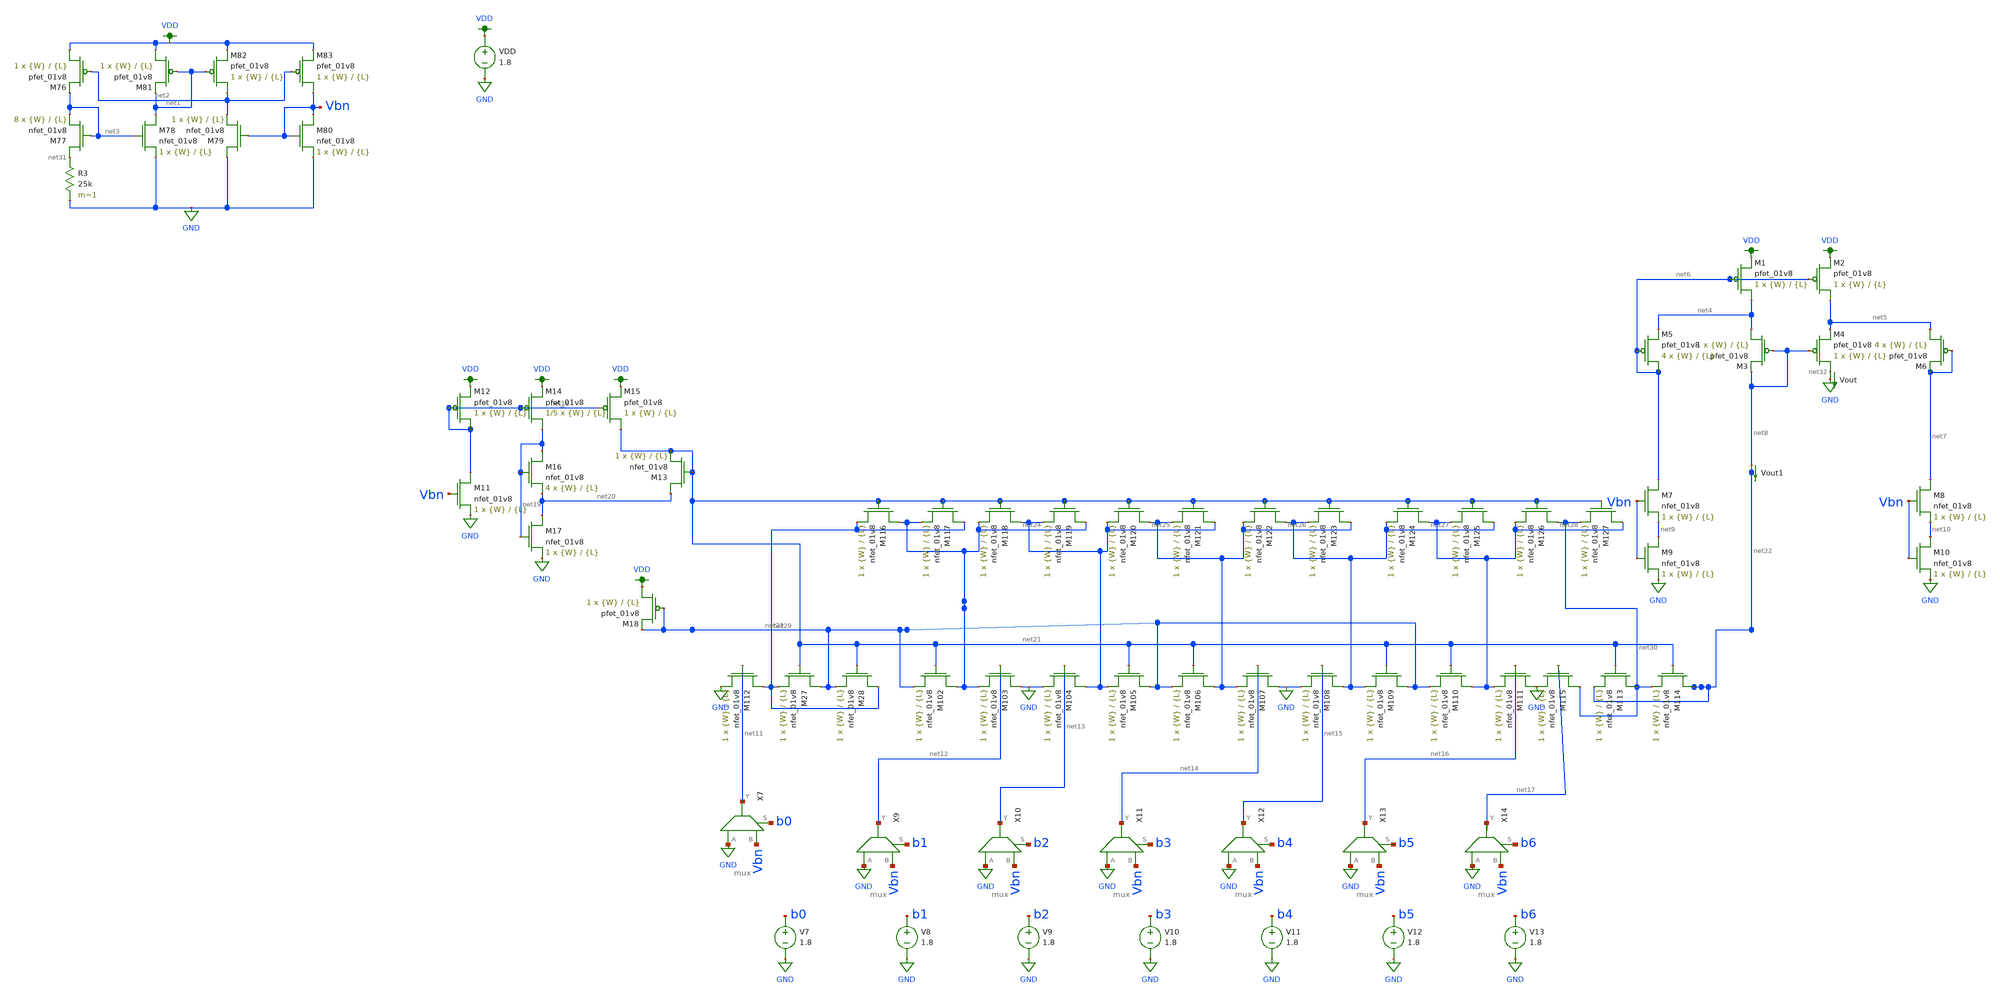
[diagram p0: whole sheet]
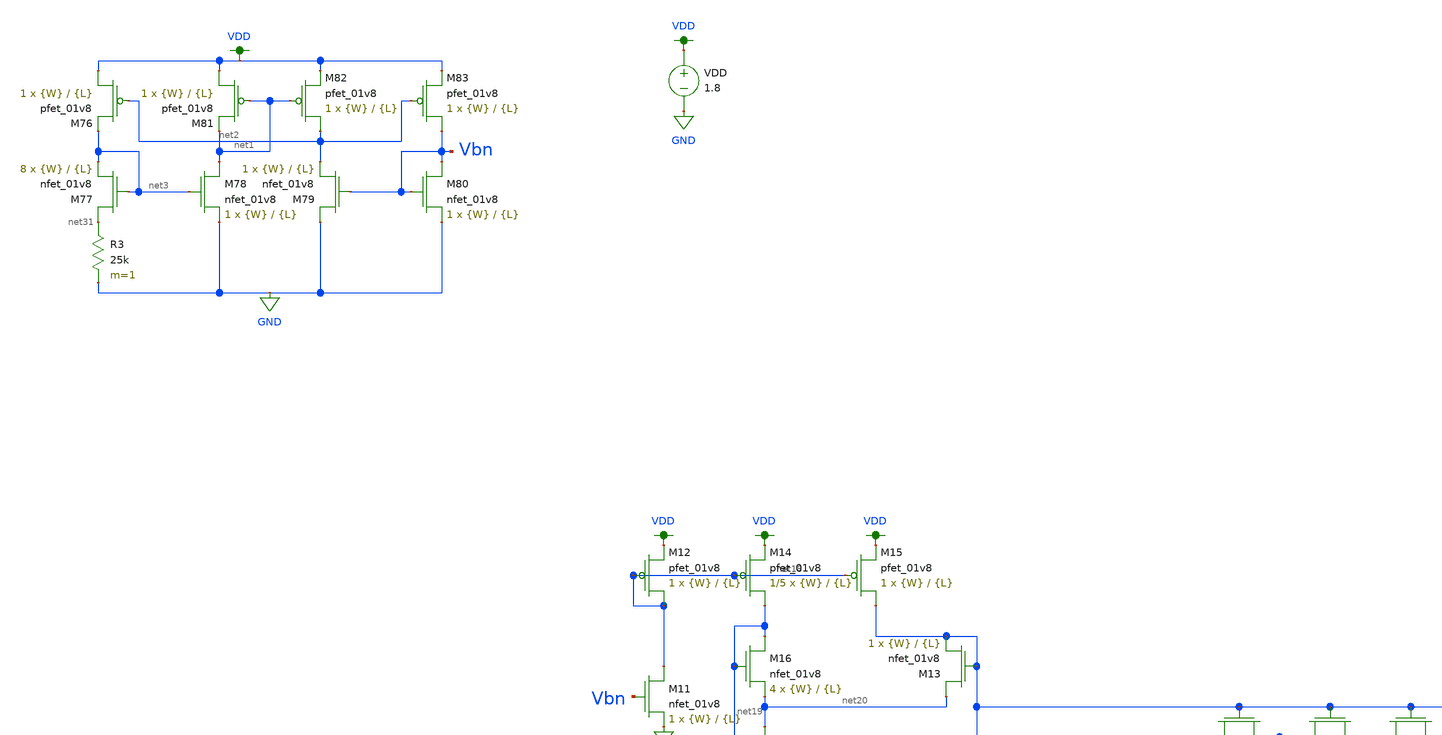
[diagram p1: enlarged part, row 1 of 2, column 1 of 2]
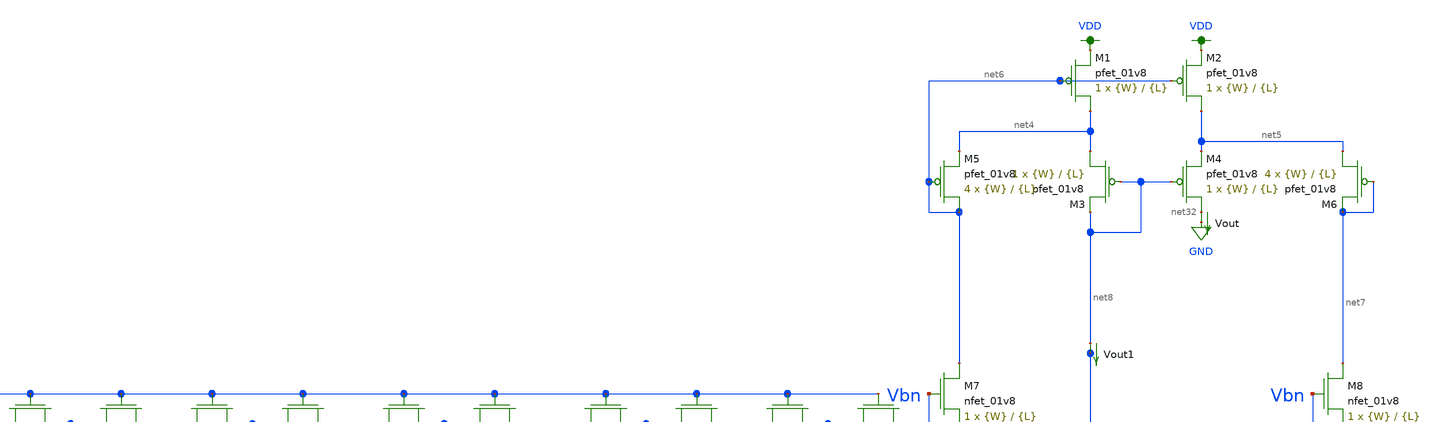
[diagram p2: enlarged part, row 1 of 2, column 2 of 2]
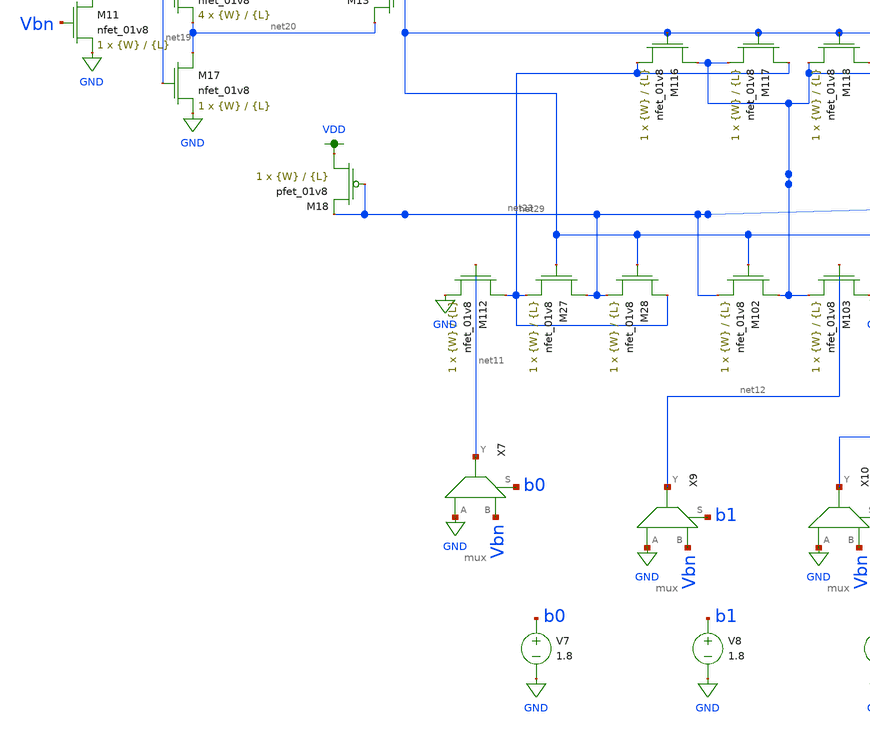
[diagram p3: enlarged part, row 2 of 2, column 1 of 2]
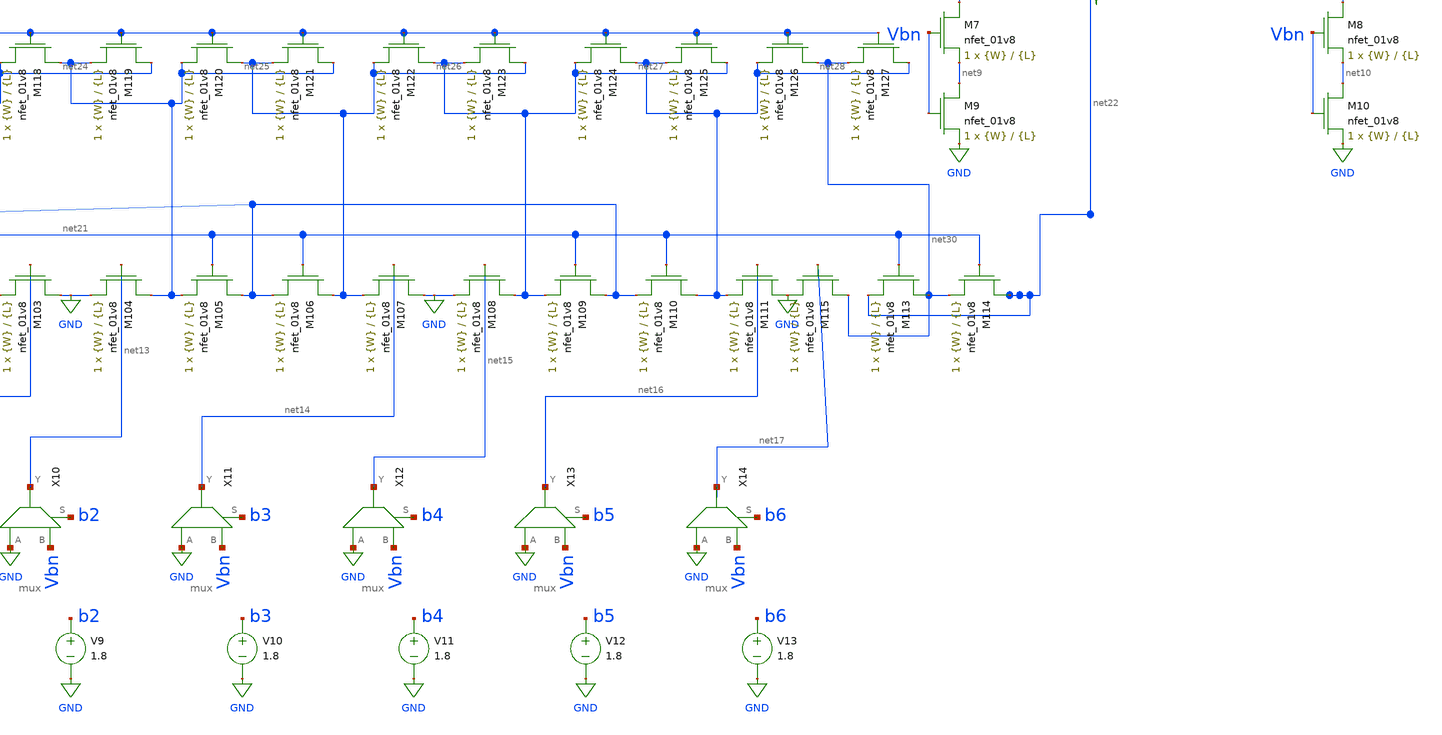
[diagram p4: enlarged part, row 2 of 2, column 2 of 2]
** sch_path: dac/schematics/misc/lds_temp.sch
**.subckt lds_temp
VDD VDD GND 1.8
XM76 VDD net2 net3 VDD sky130_fd_pr__pfet_01v8 L={L} W={W} nf=1 ad='int((nf+1)/2) * W/nf * 0.29' as='int((nf+2)/2) * W/nf * 0.29'
+ pd='2*int((nf+1)/2) * (W/nf + 0.29)' ps='2*int((nf+2)/2) * (W/nf + 0.29)' nrd='0.29 / W' nrs='0.29 / W'
+ sa=0 sb=0 sd=0 mult=1 m=1
XM77 net31 net3 net3 GND sky130_fd_pr__nfet_01v8 L={L} W={W} nf=1 ad='int((nf+1)/2) * W/nf * 0.29' as='int((nf+2)/2) * W/nf * 0.29'
+ pd='2*int((nf+1)/2) * (W/nf + 0.29)' ps='2*int((nf+2)/2) * (W/nf + 0.29)' nrd='0.29 / W' nrs='0.29 / W'
+ sa=0 sb=0 sd=0 mult=8 m=8
R3 net31 GND 25k m=1
XM78 net1 net3 GND GND sky130_fd_pr__nfet_01v8 L={L} W={W} nf=1 ad='int((nf+1)/2) * W/nf * 0.29' as='int((nf+2)/2) * W/nf * 0.29'
+ pd='2*int((nf+1)/2) * (W/nf + 0.29)' ps='2*int((nf+2)/2) * (W/nf + 0.29)' nrd='0.29 / W' nrs='0.29 / W'
+ sa=0 sb=0 sd=0 mult=1 m=1
XM79 GND Vbn net2 GND sky130_fd_pr__nfet_01v8 L={L} W={W} nf=1 ad='int((nf+1)/2) * W/nf * 0.29' as='int((nf+2)/2) * W/nf * 0.29'
+ pd='2*int((nf+1)/2) * (W/nf + 0.29)' ps='2*int((nf+2)/2) * (W/nf + 0.29)' nrd='0.29 / W' nrs='0.29 / W'
+ sa=0 sb=0 sd=0 mult=1 m=1
XM80 Vbn Vbn GND GND sky130_fd_pr__nfet_01v8 L={L} W={W} nf=1 ad='int((nf+1)/2) * W/nf * 0.29' as='int((nf+2)/2) * W/nf * 0.29'
+ pd='2*int((nf+1)/2) * (W/nf + 0.29)' ps='2*int((nf+2)/2) * (W/nf + 0.29)' nrd='0.29 / W' nrs='0.29 / W'
+ sa=0 sb=0 sd=0 mult=1 m=1
XM81 VDD net1 net1 VDD sky130_fd_pr__pfet_01v8 L={L} W={W} nf=1 ad='int((nf+1)/2) * W/nf * 0.29' as='int((nf+2)/2) * W/nf * 0.29'
+ pd='2*int((nf+1)/2) * (W/nf + 0.29)' ps='2*int((nf+2)/2) * (W/nf + 0.29)' nrd='0.29 / W' nrs='0.29 / W'
+ sa=0 sb=0 sd=0 mult=1 m=1
XM82 net2 net1 VDD VDD sky130_fd_pr__pfet_01v8 L={L} W={W} nf=1 ad='int((nf+1)/2) * W/nf * 0.29' as='int((nf+2)/2) * W/nf * 0.29'
+ pd='2*int((nf+1)/2) * (W/nf + 0.29)' ps='2*int((nf+2)/2) * (W/nf + 0.29)' nrd='0.29 / W' nrs='0.29 / W'
+ sa=0 sb=0 sd=0 mult=1 m=1
XM83 Vbn net2 VDD VDD sky130_fd_pr__pfet_01v8 L={L} W={W} nf=1 ad='int((nf+1)/2) * W/nf * 0.29' as='int((nf+2)/2) * W/nf * 0.29'
+ pd='2*int((nf+1)/2) * (W/nf + 0.29)' ps='2*int((nf+2)/2) * (W/nf + 0.29)' nrd='0.29 / W' nrs='0.29 / W'
+ sa=0 sb=0 sd=0 mult=1 m=1
Vout net32 GND 0
.save i(vout)
XM1 net4 net6 VDD VDD sky130_fd_pr__pfet_01v8 L={L} W={W} nf=1 ad='int((nf+1)/2) * W/nf * 0.29' as='int((nf+2)/2) * W/nf * 0.29'
+ pd='2*int((nf+1)/2) * (W/nf + 0.29)' ps='2*int((nf+2)/2) * (W/nf + 0.29)' nrd='0.29 / W' nrs='0.29 / W'
+ sa=0 sb=0 sd=0 mult=1 m=1
XM2 net5 net6 VDD VDD sky130_fd_pr__pfet_01v8 L={L} W={W} nf=1 ad='int((nf+1)/2) * W/nf * 0.29' as='int((nf+2)/2) * W/nf * 0.29'
+ pd='2*int((nf+1)/2) * (W/nf + 0.29)' ps='2*int((nf+2)/2) * (W/nf + 0.29)' nrd='0.29 / W' nrs='0.29 / W'
+ sa=0 sb=0 sd=0 mult=1 m=1
XM3 net4 net8 net8 VDD sky130_fd_pr__pfet_01v8 L={L} W={W} nf=1 ad='int((nf+1)/2) * W/nf * 0.29' as='int((nf+2)/2) * W/nf * 0.29'
+ pd='2*int((nf+1)/2) * (W/nf + 0.29)' ps='2*int((nf+2)/2) * (W/nf + 0.29)' nrd='0.29 / W' nrs='0.29 / W'
+ sa=0 sb=0 sd=0 mult=1 m=1
XM4 net32 net8 net5 VDD sky130_fd_pr__pfet_01v8 L={L} W={W} nf=1 ad='int((nf+1)/2) * W/nf * 0.29' as='int((nf+2)/2) * W/nf * 0.29'
+ pd='2*int((nf+1)/2) * (W/nf + 0.29)' ps='2*int((nf+2)/2) * (W/nf + 0.29)' nrd='0.29 / W' nrs='0.29 / W'
+ sa=0 sb=0 sd=0 mult=1 m=1
XM5 net6 net6 net4 VDD sky130_fd_pr__pfet_01v8 L={L} W={W} nf=1 ad='int((nf+1)/2) * W/nf * 0.29' as='int((nf+2)/2) * W/nf * 0.29'
+ pd='2*int((nf+1)/2) * (W/nf + 0.29)' ps='2*int((nf+2)/2) * (W/nf + 0.29)' nrd='0.29 / W' nrs='0.29 / W'
+ sa=0 sb=0 sd=0 mult=4 m=4
XM6 net5 net7 net7 VDD sky130_fd_pr__pfet_01v8 L={L} W={W} nf=1 ad='int((nf+1)/2) * W/nf * 0.29' as='int((nf+2)/2) * W/nf * 0.29'
+ pd='2*int((nf+1)/2) * (W/nf + 0.29)' ps='2*int((nf+2)/2) * (W/nf + 0.29)' nrd='0.29 / W' nrs='0.29 / W'
+ sa=0 sb=0 sd=0 mult=4 m=4
XM7 net6 Vbn net9 GND sky130_fd_pr__nfet_01v8 L={L} W={W} nf=1 ad='int((nf+1)/2) * W/nf * 0.29' as='int((nf+2)/2) * W/nf * 0.29'
+ pd='2*int((nf+1)/2) * (W/nf + 0.29)' ps='2*int((nf+2)/2) * (W/nf + 0.29)' nrd='0.29 / W' nrs='0.29 / W'
+ sa=0 sb=0 sd=0 mult=1 m=1
XM8 net7 Vbn net10 GND sky130_fd_pr__nfet_01v8 L={L} W={W} nf=1 ad='int((nf+1)/2) * W/nf * 0.29' as='int((nf+2)/2) * W/nf * 0.29'
+ pd='2*int((nf+1)/2) * (W/nf + 0.29)' ps='2*int((nf+2)/2) * (W/nf + 0.29)' nrd='0.29 / W' nrs='0.29 / W'
+ sa=0 sb=0 sd=0 mult=1 m=1
XM9 net9 Vbn GND GND sky130_fd_pr__nfet_01v8 L={L} W={W} nf=1 ad='int((nf+1)/2) * W/nf * 0.29' as='int((nf+2)/2) * W/nf * 0.29'
+ pd='2*int((nf+1)/2) * (W/nf + 0.29)' ps='2*int((nf+2)/2) * (W/nf + 0.29)' nrd='0.29 / W' nrs='0.29 / W'
+ sa=0 sb=0 sd=0 mult=1 m=1
XM10 net10 Vbn GND GND sky130_fd_pr__nfet_01v8 L={L} W={W} nf=1 ad='int((nf+1)/2) * W/nf * 0.29' as='int((nf+2)/2) * W/nf * 0.29'
+ pd='2*int((nf+1)/2) * (W/nf + 0.29)' ps='2*int((nf+2)/2) * (W/nf + 0.29)' nrd='0.29 / W' nrs='0.29 / W'
+ sa=0 sb=0 sd=0 mult=1 m=1
V7 b0 GND 1.8
V8 b1 GND 1.8
V9 b2 GND 1.8
V10 b3 GND 1.8
V11 b4 GND 1.8
V12 b5 GND 1.8
V13 b6 GND 1.8
X7 GND Vbn net11 b0 mux
X9 GND Vbn net12 b1 mux
X10 GND Vbn net13 b2 mux
X11 GND Vbn net14 b3 mux
X12 GND Vbn net15 b4 mux
X13 GND Vbn net16 b5 mux
X14 GND Vbn net17 b6 mux
XM11 net18 Vbn GND GND sky130_fd_pr__nfet_01v8 L={L} W={W} nf=1 ad='int((nf+1)/2) * W/nf * 0.29' as='int((nf+2)/2) * W/nf * 0.29'
+ pd='2*int((nf+1)/2) * (W/nf + 0.29)' ps='2*int((nf+2)/2) * (W/nf + 0.29)' nrd='0.29 / W' nrs='0.29 / W'
+ sa=0 sb=0 sd=0 mult=1 m=1
XM12 net18 net18 VDD VDD sky130_fd_pr__pfet_01v8 L={L} W={W} nf=1 ad='int((nf+1)/2) * W/nf * 0.29' as='int((nf+2)/2) * W/nf * 0.29'
+ pd='2*int((nf+1)/2) * (W/nf + 0.29)' ps='2*int((nf+2)/2) * (W/nf + 0.29)' nrd='0.29 / W' nrs='0.29 / W'
+ sa=0 sb=0 sd=0 mult=1 m=1
XM13 net20 net21 net21 GND sky130_fd_pr__nfet_01v8 L={L} W={W} nf=1 ad='int((nf+1)/2) * W/nf * 0.29'
+ as='int((nf+2)/2) * W/nf * 0.29' pd='2*int((nf+1)/2) * (W/nf + 0.29)' ps='2*int((nf+2)/2) * (W/nf + 0.29)'
+ nrd='0.29 / W' nrs='0.29 / W' sa=0 sb=0 sd=0 mult=1 m=1
XM14 net19 net18 VDD VDD sky130_fd_pr__pfet_01v8 L={L} W={W} nf=1 ad='int((nf+1)/2) * W/nf * 0.29' as='int((nf+2)/2) * W/nf * 0.29'
+ pd='2*int((nf+1)/2) * (W/nf + 0.29)' ps='2*int((nf+2)/2) * (W/nf + 0.29)' nrd='0.29 / W' nrs='0.29 / W'
+ sa=0 sb=0 sd=0 mult=1/5 m=1/5
XM15 net21 net18 VDD VDD sky130_fd_pr__pfet_01v8 L={L} W={W} nf=1 ad='int((nf+1)/2) * W/nf * 0.29' as='int((nf+2)/2) * W/nf * 0.29'
+ pd='2*int((nf+1)/2) * (W/nf + 0.29)' ps='2*int((nf+2)/2) * (W/nf + 0.29)' nrd='0.29 / W' nrs='0.29 / W'
+ sa=0 sb=0 sd=0 mult=1 m=1
XM16 net19 net19 net20 GND sky130_fd_pr__nfet_01v8 L={L} W={W} nf=1 ad='int((nf+1)/2) * W/nf * 0.29'
+ as='int((nf+2)/2) * W/nf * 0.29' pd='2*int((nf+1)/2) * (W/nf + 0.29)' ps='2*int((nf+2)/2) * (W/nf + 0.29)'
+ nrd='0.29 / W' nrs='0.29 / W' sa=0 sb=0 sd=0 mult=4 m=4
XM17 net20 net19 GND GND sky130_fd_pr__nfet_01v8 L={L} W={W} nf=1 ad='int((nf+1)/2) * W/nf * 0.29' as='int((nf+2)/2) * W/nf * 0.29'
+ pd='2*int((nf+1)/2) * (W/nf + 0.29)' ps='2*int((nf+2)/2) * (W/nf + 0.29)' nrd='0.29 / W' nrs='0.29 / W'
+ sa=0 sb=0 sd=0 mult=1 m=1
Vout1 net8 net22 0
.save i(vout1)
XM18 VDD net23 net23 VDD sky130_fd_pr__pfet_01v8 L={L} W={W} nf=1 ad='int((nf+1)/2) * W/nf * 0.29' as='int((nf+2)/2) * W/nf * 0.29'
+ pd='2*int((nf+1)/2) * (W/nf + 0.29)' ps='2*int((nf+2)/2) * (W/nf + 0.29)' nrd='0.29 / W' nrs='0.29 / W'
+ sa=0 sb=0 sd=0 mult=1 m=1
XM27 net23 net21 net29 GND sky130_fd_pr__nfet_01v8 L={L} W={W} nf=1 ad='int((nf+1)/2) * W/nf * 0.29'
+ as='int((nf+2)/2) * W/nf * 0.29' pd='2*int((nf+1)/2) * (W/nf + 0.29)' ps='2*int((nf+2)/2) * (W/nf + 0.29)'
+ nrd='0.29 / W' nrs='0.29 / W' sa=0 sb=0 sd=0 mult=1 m=1
XM28 net29 net21 net23 GND sky130_fd_pr__nfet_01v8 L={L} W={W} nf=1 ad='int((nf+1)/2) * W/nf * 0.29'
+ as='int((nf+2)/2) * W/nf * 0.29' pd='2*int((nf+1)/2) * (W/nf + 0.29)' ps='2*int((nf+2)/2) * (W/nf + 0.29)'
+ nrd='0.29 / W' nrs='0.29 / W' sa=0 sb=0 sd=0 mult=1 m=1
XM102 net24 net21 net23 GND sky130_fd_pr__nfet_01v8 L={L} W={W} nf=1 ad='int((nf+1)/2) * W/nf * 0.29'
+ as='int((nf+2)/2) * W/nf * 0.29' pd='2*int((nf+1)/2) * (W/nf + 0.29)' ps='2*int((nf+2)/2) * (W/nf + 0.29)'
+ nrd='0.29 / W' nrs='0.29 / W' sa=0 sb=0 sd=0 mult=1 m=1
XM103 GND net12 net24 GND sky130_fd_pr__nfet_01v8 L={L} W={W} nf=1 ad='int((nf+1)/2) * W/nf * 0.29' as='int((nf+2)/2) * W/nf * 0.29'
+ pd='2*int((nf+1)/2) * (W/nf + 0.29)' ps='2*int((nf+2)/2) * (W/nf + 0.29)' nrd='0.29 / W' nrs='0.29 / W'
+ sa=0 sb=0 sd=0 mult=1 m=1
XM104 net25 net13 GND GND sky130_fd_pr__nfet_01v8 L={L} W={W} nf=1 ad='int((nf+1)/2) * W/nf * 0.29' as='int((nf+2)/2) * W/nf * 0.29'
+ pd='2*int((nf+1)/2) * (W/nf + 0.29)' ps='2*int((nf+2)/2) * (W/nf + 0.29)' nrd='0.29 / W' nrs='0.29 / W'
+ sa=0 sb=0 sd=0 mult=1 m=1
XM105 net23 net21 net25 GND sky130_fd_pr__nfet_01v8 L={L} W={W} nf=1 ad='int((nf+1)/2) * W/nf * 0.29'
+ as='int((nf+2)/2) * W/nf * 0.29' pd='2*int((nf+1)/2) * (W/nf + 0.29)' ps='2*int((nf+2)/2) * (W/nf + 0.29)'
+ nrd='0.29 / W' nrs='0.29 / W' sa=0 sb=0 sd=0 mult=1 m=1
XM106 net26 net21 net23 GND sky130_fd_pr__nfet_01v8 L={L} W={W} nf=1 ad='int((nf+1)/2) * W/nf * 0.29'
+ as='int((nf+2)/2) * W/nf * 0.29' pd='2*int((nf+1)/2) * (W/nf + 0.29)' ps='2*int((nf+2)/2) * (W/nf + 0.29)'
+ nrd='0.29 / W' nrs='0.29 / W' sa=0 sb=0 sd=0 mult=1 m=1
XM107 GND net14 net26 GND sky130_fd_pr__nfet_01v8 L={L} W={W} nf=1 ad='int((nf+1)/2) * W/nf * 0.29' as='int((nf+2)/2) * W/nf * 0.29'
+ pd='2*int((nf+1)/2) * (W/nf + 0.29)' ps='2*int((nf+2)/2) * (W/nf + 0.29)' nrd='0.29 / W' nrs='0.29 / W'
+ sa=0 sb=0 sd=0 mult=1 m=1
XM108 net27 net15 GND GND sky130_fd_pr__nfet_01v8 L={L} W={W} nf=1 ad='int((nf+1)/2) * W/nf * 0.29' as='int((nf+2)/2) * W/nf * 0.29'
+ pd='2*int((nf+1)/2) * (W/nf + 0.29)' ps='2*int((nf+2)/2) * (W/nf + 0.29)' nrd='0.29 / W' nrs='0.29 / W'
+ sa=0 sb=0 sd=0 mult=1 m=1
XM109 net23 net21 net27 GND sky130_fd_pr__nfet_01v8 L={L} W={W} nf=1 ad='int((nf+1)/2) * W/nf * 0.29'
+ as='int((nf+2)/2) * W/nf * 0.29' pd='2*int((nf+1)/2) * (W/nf + 0.29)' ps='2*int((nf+2)/2) * (W/nf + 0.29)'
+ nrd='0.29 / W' nrs='0.29 / W' sa=0 sb=0 sd=0 mult=1 m=1
XM110 net28 net21 net23 GND sky130_fd_pr__nfet_01v8 L={L} W={W} nf=1 ad='int((nf+1)/2) * W/nf * 0.29'
+ as='int((nf+2)/2) * W/nf * 0.29' pd='2*int((nf+1)/2) * (W/nf + 0.29)' ps='2*int((nf+2)/2) * (W/nf + 0.29)'
+ nrd='0.29 / W' nrs='0.29 / W' sa=0 sb=0 sd=0 mult=1 m=1
XM111 GND net16 net28 GND sky130_fd_pr__nfet_01v8 L={L} W={W} nf=1 ad='int((nf+1)/2) * W/nf * 0.29' as='int((nf+2)/2) * W/nf * 0.29'
+ pd='2*int((nf+1)/2) * (W/nf + 0.29)' ps='2*int((nf+2)/2) * (W/nf + 0.29)' nrd='0.29 / W' nrs='0.29 / W'
+ sa=0 sb=0 sd=0 mult=1 m=1
XM112 net29 net11 GND GND sky130_fd_pr__nfet_01v8 L={L} W={W} nf=1 ad='int((nf+1)/2) * W/nf * 0.29' as='int((nf+2)/2) * W/nf * 0.29'
+ pd='2*int((nf+1)/2) * (W/nf + 0.29)' ps='2*int((nf+2)/2) * (W/nf + 0.29)' nrd='0.29 / W' nrs='0.29 / W'
+ sa=0 sb=0 sd=0 mult=1 m=1
XM113 net30 net21 net22 GND sky130_fd_pr__nfet_01v8 L={L} W={W} nf=1 ad='int((nf+1)/2) * W/nf * 0.29'
+ as='int((nf+2)/2) * W/nf * 0.29' pd='2*int((nf+1)/2) * (W/nf + 0.29)' ps='2*int((nf+2)/2) * (W/nf + 0.29)'
+ nrd='0.29 / W' nrs='0.29 / W' sa=0 sb=0 sd=0 mult=1 m=1
XM114 net22 net21 net30 GND sky130_fd_pr__nfet_01v8 L={L} W={W} nf=1 ad='int((nf+1)/2) * W/nf * 0.29'
+ as='int((nf+2)/2) * W/nf * 0.29' pd='2*int((nf+1)/2) * (W/nf + 0.29)' ps='2*int((nf+2)/2) * (W/nf + 0.29)'
+ nrd='0.29 / W' nrs='0.29 / W' sa=0 sb=0 sd=0 mult=1 m=1
XM115 net30 net17 GND GND sky130_fd_pr__nfet_01v8 L={L} W={W} nf=1 ad='int((nf+1)/2) * W/nf * 0.29' as='int((nf+2)/2) * W/nf * 0.29'
+ pd='2*int((nf+1)/2) * (W/nf + 0.29)' ps='2*int((nf+2)/2) * (W/nf + 0.29)' nrd='0.29 / W' nrs='0.29 / W'
+ sa=0 sb=0 sd=0 mult=1 m=1
XM116 net24 net21 net29 GND sky130_fd_pr__nfet_01v8 L={L} W={W} nf=1 ad='int((nf+1)/2) * W/nf * 0.29'
+ as='int((nf+2)/2) * W/nf * 0.29' pd='2*int((nf+1)/2) * (W/nf + 0.29)' ps='2*int((nf+2)/2) * (W/nf + 0.29)'
+ nrd='0.29 / W' nrs='0.29 / W' sa=0 sb=0 sd=0 mult=1 m=1
XM117 net29 net21 net24 GND sky130_fd_pr__nfet_01v8 L={L} W={W} nf=1 ad='int((nf+1)/2) * W/nf * 0.29'
+ as='int((nf+2)/2) * W/nf * 0.29' pd='2*int((nf+1)/2) * (W/nf + 0.29)' ps='2*int((nf+2)/2) * (W/nf + 0.29)'
+ nrd='0.29 / W' nrs='0.29 / W' sa=0 sb=0 sd=0 mult=1 m=1
XM118 net25 net21 net24 GND sky130_fd_pr__nfet_01v8 L={L} W={W} nf=1 ad='int((nf+1)/2) * W/nf * 0.29'
+ as='int((nf+2)/2) * W/nf * 0.29' pd='2*int((nf+1)/2) * (W/nf + 0.29)' ps='2*int((nf+2)/2) * (W/nf + 0.29)'
+ nrd='0.29 / W' nrs='0.29 / W' sa=0 sb=0 sd=0 mult=1 m=1
XM119 net24 net21 net25 GND sky130_fd_pr__nfet_01v8 L={L} W={W} nf=1 ad='int((nf+1)/2) * W/nf * 0.29'
+ as='int((nf+2)/2) * W/nf * 0.29' pd='2*int((nf+1)/2) * (W/nf + 0.29)' ps='2*int((nf+2)/2) * (W/nf + 0.29)'
+ nrd='0.29 / W' nrs='0.29 / W' sa=0 sb=0 sd=0 mult=1 m=1
XM120 net26 net21 net25 GND sky130_fd_pr__nfet_01v8 L={L} W={W} nf=1 ad='int((nf+1)/2) * W/nf * 0.29'
+ as='int((nf+2)/2) * W/nf * 0.29' pd='2*int((nf+1)/2) * (W/nf + 0.29)' ps='2*int((nf+2)/2) * (W/nf + 0.29)'
+ nrd='0.29 / W' nrs='0.29 / W' sa=0 sb=0 sd=0 mult=1 m=1
XM121 net25 net21 net26 GND sky130_fd_pr__nfet_01v8 L={L} W={W} nf=1 ad='int((nf+1)/2) * W/nf * 0.29'
+ as='int((nf+2)/2) * W/nf * 0.29' pd='2*int((nf+1)/2) * (W/nf + 0.29)' ps='2*int((nf+2)/2) * (W/nf + 0.29)'
+ nrd='0.29 / W' nrs='0.29 / W' sa=0 sb=0 sd=0 mult=1 m=1
XM122 net27 net21 net26 GND sky130_fd_pr__nfet_01v8 L={L} W={W} nf=1 ad='int((nf+1)/2) * W/nf * 0.29'
+ as='int((nf+2)/2) * W/nf * 0.29' pd='2*int((nf+1)/2) * (W/nf + 0.29)' ps='2*int((nf+2)/2) * (W/nf + 0.29)'
+ nrd='0.29 / W' nrs='0.29 / W' sa=0 sb=0 sd=0 mult=1 m=1
XM123 net26 net21 net27 GND sky130_fd_pr__nfet_01v8 L={L} W={W} nf=1 ad='int((nf+1)/2) * W/nf * 0.29'
+ as='int((nf+2)/2) * W/nf * 0.29' pd='2*int((nf+1)/2) * (W/nf + 0.29)' ps='2*int((nf+2)/2) * (W/nf + 0.29)'
+ nrd='0.29 / W' nrs='0.29 / W' sa=0 sb=0 sd=0 mult=1 m=1
XM124 net28 net21 net27 GND sky130_fd_pr__nfet_01v8 L={L} W={W} nf=1 ad='int((nf+1)/2) * W/nf * 0.29'
+ as='int((nf+2)/2) * W/nf * 0.29' pd='2*int((nf+1)/2) * (W/nf + 0.29)' ps='2*int((nf+2)/2) * (W/nf + 0.29)'
+ nrd='0.29 / W' nrs='0.29 / W' sa=0 sb=0 sd=0 mult=1 m=1
XM125 net27 net21 net28 GND sky130_fd_pr__nfet_01v8 L={L} W={W} nf=1 ad='int((nf+1)/2) * W/nf * 0.29'
+ as='int((nf+2)/2) * W/nf * 0.29' pd='2*int((nf+1)/2) * (W/nf + 0.29)' ps='2*int((nf+2)/2) * (W/nf + 0.29)'
+ nrd='0.29 / W' nrs='0.29 / W' sa=0 sb=0 sd=0 mult=1 m=1
XM126 net30 net21 net28 GND sky130_fd_pr__nfet_01v8 L={L} W={W} nf=1 ad='int((nf+1)/2) * W/nf * 0.29'
+ as='int((nf+2)/2) * W/nf * 0.29' pd='2*int((nf+1)/2) * (W/nf + 0.29)' ps='2*int((nf+2)/2) * (W/nf + 0.29)'
+ nrd='0.29 / W' nrs='0.29 / W' sa=0 sb=0 sd=0 mult=1 m=1
XM127 net28 net21 net30 GND sky130_fd_pr__nfet_01v8 L={L} W={W} nf=1 ad='int((nf+1)/2) * W/nf * 0.29'
+ as='int((nf+2)/2) * W/nf * 0.29' pd='2*int((nf+1)/2) * (W/nf + 0.29)' ps='2*int((nf+2)/2) * (W/nf + 0.29)'
+ nrd='0.29 / W' nrs='0.29 / W' sa=0 sb=0 sd=0 mult=1 m=1
**** begin user architecture code

.param W=32
.param L=4
.control
set wr_vecnames
set wr_singlescale
let code = 0
  while code < 128
    if code eq 0
      let b0 = 0
    else
      let b0 = code % 2 * 1.8
    end
    if floor(code / 2) eq 0
      let b1 = 0
    else
      let b1 = floor(code / 2) % 2 * 1.8
    end
    if floor(code / 4) eq 0
      let b2 = 0
    else
      let b2 = floor(code / 4) % 2 * 1.8
    end
    if floor(code / 8) eq 0
      let b3 = 0
    else
      let b3 = floor(code / 8) % 2 * 1.8
    end
    if floor(code / 16) eq 0
      let b4 = 0
    else
      let b4 = floor(code / 16) % 2 * 1.8
    end
    if floor(code / 32) eq 0
      let b5 = 0
    else
      let b5 = floor(code / 32) % 2 * 1.8
    end
    if floor(code / 64) eq 0
      let b6 = 0
    else
      let b6 = floor(code / 64) % 2 * 1.8
    end
    alter v7 $&b0
    alter v8 $&b1
    alter v9 $&b2
    alter v10 $&b3
    alter v11 $&b4
    alter v12 $&b5
    alter v13 $&b6
    save all
    op
    wrdata ~/Documents/current-output-dac-vlsi/simulations/dac_sim.txt v(Vbn) i(Vout) i(Vout1) v(b6)
+ v(b5) v(b4) v(b3) v(b2) v(b1) v(b0)
    if code eq 0
      set appendwrite
      set wr_vecnames = FALSE
    end
    let code = code + 1
  end
.endc


.option wnflag=1
.param MC_SWITCH=1.0
.lib ~/skywater/skywater-pdk/libraries/sky130_fd_pr_ngspice/latest/models/sky130.lib.spice tt

**** end user architecture code
**.ends

* expanding   symbol:  /home/madvlsi/Documents/current-output-dac-vlsi/schematics/mux.sym # of
*+ pins=4
** sym_path: dac/schematics/mux.sym
** sch_path: dac/schematics/mux.sch
.subckt mux A B Y S
*.ipin A
*.ipin B
*.ipin S
*.opin Y
XM1 A S Y VDD sky130_fd_pr__pfet_01v8 L=0.15 W=1 nf=1 ad='int((nf+1)/2) * W/nf * 0.29' as='int((nf+2)/2) * W/nf * 0.29'
+ pd='2*int((nf+1)/2) * (W/nf + 0.29)' ps='2*int((nf+2)/2) * (W/nf + 0.29)' nrd='0.29 / W' nrs='0.29 / W'
+ sa=0 sb=0 sd=0 mult=1 m=1
XM3 net1 S VDD VDD sky130_fd_pr__pfet_01v8 L=0.15 W=1 nf=1 ad='int((nf+1)/2) * W/nf * 0.29' as='int((nf+2)/2) * W/nf * 0.29'
+ pd='2*int((nf+1)/2) * (W/nf + 0.29)' ps='2*int((nf+2)/2) * (W/nf + 0.29)' nrd='0.29 / W' nrs='0.29 / W'
+ sa=0 sb=0 sd=0 mult=1 m=1
XM4 net1 S GND GND sky130_fd_pr__nfet_01v8 L=0.15 W=1 nf=1 ad='int((nf+1)/2) * W/nf * 0.29' as='int((nf+2)/2) * W/nf * 0.29'
+ pd='2*int((nf+1)/2) * (W/nf + 0.29)' ps='2*int((nf+2)/2) * (W/nf + 0.29)' nrd='0.29 / W' nrs='0.29 / W'
+ sa=0 sb=0 sd=0 mult=1 m=1
XM5 A net1 Y GND sky130_fd_pr__nfet_01v8 L=0.15 W=1 nf=1 ad='int((nf+1)/2) * W/nf * 0.29' as='int((nf+2)/2) * W/nf * 0.29'
+ pd='2*int((nf+1)/2) * (W/nf + 0.29)' ps='2*int((nf+2)/2) * (W/nf + 0.29)' nrd='0.29 / W' nrs='0.29 / W'
+ sa=0 sb=0 sd=0 mult=1 m=1
XM2 B net1 Y VDD sky130_fd_pr__pfet_01v8 L=0.15 W=1 nf=1 ad='int((nf+1)/2) * W/nf * 0.29' as='int((nf+2)/2) * W/nf * 0.29'
+ pd='2*int((nf+1)/2) * (W/nf + 0.29)' ps='2*int((nf+2)/2) * (W/nf + 0.29)' nrd='0.29 / W' nrs='0.29 / W'
+ sa=0 sb=0 sd=0 mult=1 m=1
XM6 B S Y GND sky130_fd_pr__nfet_01v8 L=0.15 W=1 nf=1 ad='int((nf+1)/2) * W/nf * 0.29' as='int((nf+2)/2) * W/nf * 0.29'
+ pd='2*int((nf+1)/2) * (W/nf + 0.29)' ps='2*int((nf+2)/2) * (W/nf + 0.29)' nrd='0.29 / W' nrs='0.29 / W'
+ sa=0 sb=0 sd=0 mult=1 m=1
.ends

.GLOBAL GND
.GLOBAL VDD
.end
